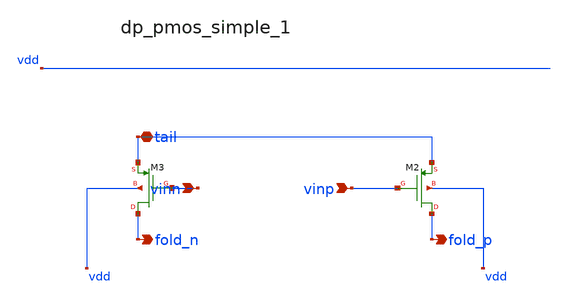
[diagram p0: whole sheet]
** sch_path: analog-db/raw/amp_026_fan_chopper_ota/hier/blocks/dp_pmos_simple_1.sch
**.subckt dp_pmos_simple_1 vinn vinp tail fold_n fold_p
*.ipin vinn
*.ipin vinp
*.iopin tail
*.opin fold_n
*.opin fold_p
XM2 fold_p vinp tail vdd sg13_lv_pmos w=x_dut_xm2_w l=x_dut_xm2_l ng=1 m=x_dut_xm2_m
XM3 fold_n vinn tail vdd sg13_lv_pmos w=x_dut_xm3_w l=x_dut_xm3_l ng=1 m=x_dut_xm3_m
**.ends
.end
